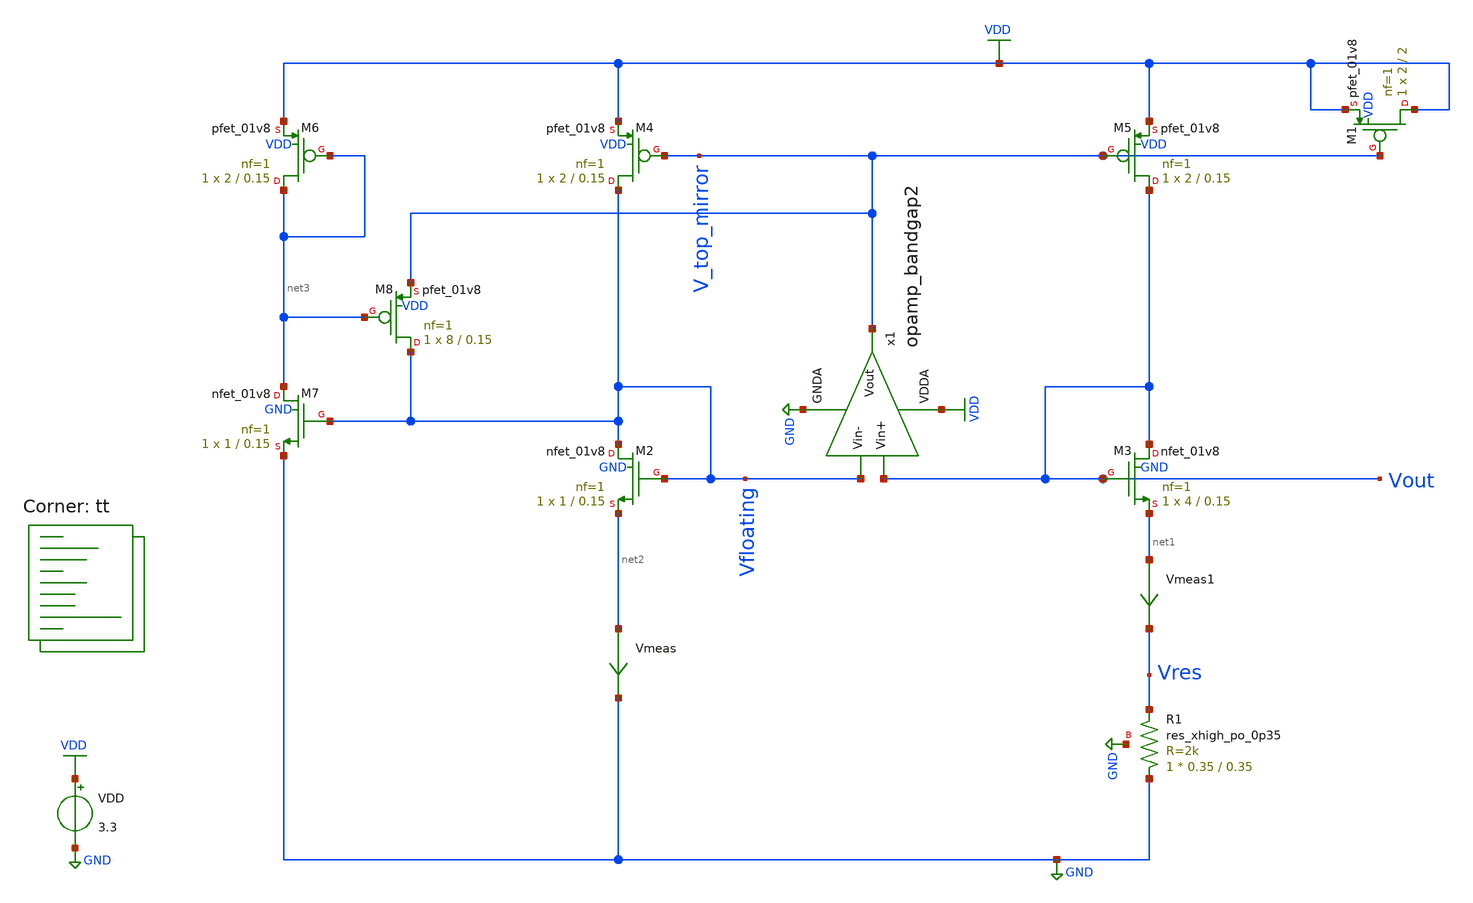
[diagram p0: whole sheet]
** sch_path: projects/bandgapref/xschem_ngspice/old_files/mos_bandgap_baker1.sch
**.subckt mos_bandgap_baker1
XM2 Vfloating Vfloating net2 GND sky130_fd_pr__nfet_01v8 L=0.15 W=1 nf=1 ad='int((nf+1)/2) * W/nf * 0.29'
+ as='int((nf+2)/2) * W/nf * 0.29' pd='2*int((nf+1)/2) * (W/nf + 0.29)' ps='2*int((nf+2)/2) * (W/nf + 0.29)'
+ nrd='0.29 / W' nrs='0.29 / W' sa=0 sb=0 sd=0 mult=1 m=1
XM3 Vout Vout net1 GND sky130_fd_pr__nfet_01v8 L=0.15 W=4 nf=1 ad='int((nf+1)/2) * W/nf * 0.29' as='int((nf+2)/2) * W/nf * 0.29'
+ pd='2*int((nf+1)/2) * (W/nf + 0.29)' ps='2*int((nf+2)/2) * (W/nf + 0.29)' nrd='0.29 / W' nrs='0.29 / W'
+ sa=0 sb=0 sd=0 mult=1 m=1
XM4 Vfloating V_top_mirror VDD VDD sky130_fd_pr__pfet_01v8 L=0.15 W=2 nf=1 ad='int((nf+1)/2) * W/nf * 0.29'
+ as='int((nf+2)/2) * W/nf * 0.29' pd='2*int((nf+1)/2) * (W/nf + 0.29)' ps='2*int((nf+2)/2) * (W/nf + 0.29)'
+ nrd='0.29 / W' nrs='0.29 / W' sa=0 sb=0 sd=0 mult=1 m=1
XM5 Vout V_top_mirror VDD VDD sky130_fd_pr__pfet_01v8 L=0.15 W=2 nf=1 ad='int((nf+1)/2) * W/nf * 0.29'
+ as='int((nf+2)/2) * W/nf * 0.29' pd='2*int((nf+1)/2) * (W/nf + 0.29)' ps='2*int((nf+2)/2) * (W/nf + 0.29)'
+ nrd='0.29 / W' nrs='0.29 / W' sa=0 sb=0 sd=0 mult=1 m=1
VDD VDD GND 3.3
Vmeas net2 GND 0
.save i(vmeas)
Vmeas1 net1 Vres 0
.save i(vmeas1)
XR1 GND Vres GND sky130_fd_pr__res_xhigh_po_0p35 L=0.35 mult=1 m=1
XM1 VDD V_top_mirror VDD VDD sky130_fd_pr__pfet_01v8 L=2 W=2 nf=1 ad='int((nf+1)/2) * W/nf * 0.29' as='int((nf+2)/2) * W/nf * 0.29'
+ pd='2*int((nf+1)/2) * (W/nf + 0.29)' ps='2*int((nf+2)/2) * (W/nf + 0.29)' nrd='0.29 / W' nrs='0.29 / W'
+ sa=0 sb=0 sd=0 mult=1 m=1
XM6 net3 net3 VDD VDD sky130_fd_pr__pfet_01v8 L=0.15 W=2 nf=1 ad='int((nf+1)/2) * W/nf * 0.29' as='int((nf+2)/2) * W/nf * 0.29'
+ pd='2*int((nf+1)/2) * (W/nf + 0.29)' ps='2*int((nf+2)/2) * (W/nf + 0.29)' nrd='0.29 / W' nrs='0.29 / W'
+ sa=0 sb=0 sd=0 mult=1 m=1
XM7 net3 Vfloating GND GND sky130_fd_pr__nfet_01v8 L=0.15 W=1 nf=1 ad='int((nf+1)/2) * W/nf * 0.29' as='int((nf+2)/2) * W/nf * 0.29'
+ pd='2*int((nf+1)/2) * (W/nf + 0.29)' ps='2*int((nf+2)/2) * (W/nf + 0.29)' nrd='0.29 / W' nrs='0.29 / W'
+ sa=0 sb=0 sd=0 mult=1 m=1
XM8 Vfloating net3 V_top_mirror VDD sky130_fd_pr__pfet_01v8 L=0.15 W=8 nf=1 ad='int((nf+1)/2) * W/nf * 0.29'
+ as='int((nf+2)/2) * W/nf * 0.29' pd='2*int((nf+1)/2) * (W/nf + 0.29)' ps='2*int((nf+2)/2) * (W/nf + 0.29)'
+ nrd='0.29 / W' nrs='0.29 / W' sa=0 sb=0 sd=0 mult=1 m=1
x1 VDD V_top_mirror Vfloating Vout GND opamp_bandgap2
**** begin user architecture code
.lib $::SKYWATER_MODELS/sky130.lib.spice tt



.option method=gear
.option wnflag=1
.option savecurrents

.save @m.xm1.msky130_fd_pr__pfet_01v8[gm] @m.xm2.msky130_fd_pr__nfet_01v8[gm] @m.xm3.msky130_fd_pr__nfet_01v8[gm] @m.xm4.msky130_fd_pr__pfet_01v8[gm] @m.xm5.msky130_fd_pr__pfet_01v8[gm] @m.xm6.msky130_fd_pr__pfet_01v8[gm] @m.xm7.msky130_fd_pr__nfet_01v8[gm] @m.xm8.msky130_fd_pr__pfet_01v8[gm]

.control
save all
op
dc VDD 0 3.3 0.3 temp -40 120 4
* tran 4ns 40us
remzerovec
write mos_bandgap_baker1.raw
set appendwrite
.endc



**** end user architecture code
**.ends

* expanding   symbol:
*+  /foss/designs/my_design/projects/pll/bandgapref/xschem_ngspice/opamp_bandgap2.sym # of pins=5
** sym_path: projects/bandgapref/xschem_ngspice/old_files/opamp_bandgap2.sym
** sch_path: projects/bandgapref/xschem_ngspice/old_files/opamp_bandgap2.sch
.subckt opamp_bandgap2 VDDA Vout Vin- Vin+ GNDA
*.ipin Vin+
*.opin Vout
*.ipin Vin-
*.ipin GNDA
*.ipin VDDA
XM2 net2 Vin- net1 GNDA sky130_fd_pr__nfet_01v8 L=0.6 W=2 nf=2 ad='int((nf+1)/2) * W/nf * 0.29' as='int((nf+2)/2) * W/nf * 0.29'
+ pd='2*int((nf+1)/2) * (W/nf + 0.29)' ps='2*int((nf+2)/2) * (W/nf + 0.29)' nrd='0.29 / W' nrs='0.29 / W'
+ sa=0 sb=0 sd=0 mult=1 m=1
XM3 Vout Vin+ net1 GNDA sky130_fd_pr__nfet_01v8 L=0.6 W=2 nf=2 ad='int((nf+1)/2) * W/nf * 0.29' as='int((nf+2)/2) * W/nf * 0.29'
+ pd='2*int((nf+1)/2) * (W/nf + 0.29)' ps='2*int((nf+2)/2) * (W/nf + 0.29)' nrd='0.29 / W' nrs='0.29 / W'
+ sa=0 sb=0 sd=0 mult=1 m=1
XM1 net1 net1 GNDA GNDA sky130_fd_pr__nfet_01v8 L=0.6 W=4 nf=1 ad='int((nf+1)/2) * W/nf * 0.29' as='int((nf+2)/2) * W/nf * 0.29'
+ pd='2*int((nf+1)/2) * (W/nf + 0.29)' ps='2*int((nf+2)/2) * (W/nf + 0.29)' nrd='0.29 / W' nrs='0.29 / W'
+ sa=0 sb=0 sd=0 mult=1 m=1
XM4 Vout net2 VDDA VDDA sky130_fd_pr__pfet_01v8 L=0.6 W=4 nf=4 ad='int((nf+1)/2) * W/nf * 0.29' as='int((nf+2)/2) * W/nf * 0.29'
+ pd='2*int((nf+1)/2) * (W/nf + 0.29)' ps='2*int((nf+2)/2) * (W/nf + 0.29)' nrd='0.29 / W' nrs='0.29 / W'
+ sa=0 sb=0 sd=0 mult=1 m=1
XM5 net2 net2 VDDA VDDA sky130_fd_pr__pfet_01v8 L=0.6 W=4 nf=4 ad='int((nf+1)/2) * W/nf * 0.29' as='int((nf+2)/2) * W/nf * 0.29'
+ pd='2*int((nf+1)/2) * (W/nf + 0.29)' ps='2*int((nf+2)/2) * (W/nf + 0.29)' nrd='0.29 / W' nrs='0.29 / W'
+ sa=0 sb=0 sd=0 mult=1 m=1
.ends

.GLOBAL VDD
.GLOBAL GND
.end
